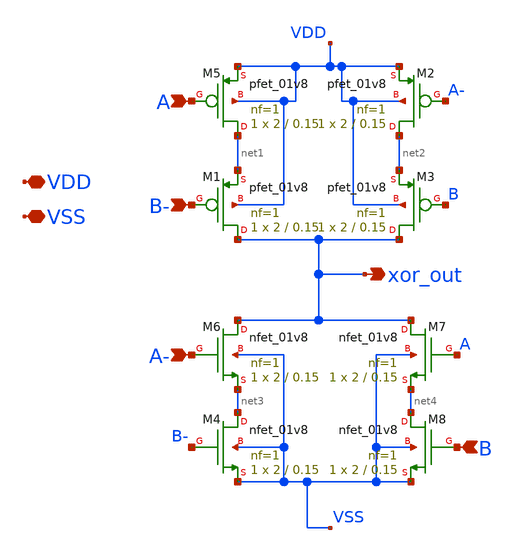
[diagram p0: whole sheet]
** sch_path: xschem/tuning/robs_xor_tune.sch
**.subckt robs_xor_tune xor_out A B- A- B VDD VSS
*.opin xor_out
*.ipin A
*.ipin B-
*.ipin A-
*.ipin B
*.iopin VDD
*.iopin VSS
XM5 net1 A VDD VDD sky130_fd_pr__pfet_01v8 L=0.15 W=2 nf=1 ad='int((nf+1)/2) * W/nf * 0.29' as='int((nf+2)/2) * W/nf * 0.29'
+ pd='2*int((nf+1)/2) * (W/nf + 0.29)' ps='2*int((nf+2)/2) * (W/nf + 0.29)' nrd='0.29 / W' nrs='0.29 / W'
+ sa=0 sb=0 sd=0 mult=1 m=1
XM6 xor_out A- net3 VSS sky130_fd_pr__nfet_01v8 L=0.15 W=2 nf=1 ad='int((nf+1)/2) * W/nf * 0.29' as='int((nf+2)/2) * W/nf * 0.29'
+ pd='2*int((nf+1)/2) * (W/nf + 0.29)' ps='2*int((nf+2)/2) * (W/nf + 0.29)' nrd='0.29 / W' nrs='0.29 / W'
+ sa=0 sb=0 sd=0 mult=1 m=1
XM1 xor_out B- net1 VDD sky130_fd_pr__pfet_01v8 L=0.15 W=2 nf=1 ad='int((nf+1)/2) * W/nf * 0.29' as='int((nf+2)/2) * W/nf * 0.29'
+ pd='2*int((nf+1)/2) * (W/nf + 0.29)' ps='2*int((nf+2)/2) * (W/nf + 0.29)' nrd='0.29 / W' nrs='0.29 / W'
+ sa=0 sb=0 sd=0 mult=1 m=1
XM2 net2 A- VDD VDD sky130_fd_pr__pfet_01v8 L=0.15 W=2 nf=1 ad='int((nf+1)/2) * W/nf * 0.29' as='int((nf+2)/2) * W/nf * 0.29'
+ pd='2*int((nf+1)/2) * (W/nf + 0.29)' ps='2*int((nf+2)/2) * (W/nf + 0.29)' nrd='0.29 / W' nrs='0.29 / W'
+ sa=0 sb=0 sd=0 mult=1 m=1
XM3 xor_out B net2 VDD sky130_fd_pr__pfet_01v8 L=0.15 W=2 nf=1 ad='int((nf+1)/2) * W/nf * 0.29' as='int((nf+2)/2) * W/nf * 0.29'
+ pd='2*int((nf+1)/2) * (W/nf + 0.29)' ps='2*int((nf+2)/2) * (W/nf + 0.29)' nrd='0.29 / W' nrs='0.29 / W'
+ sa=0 sb=0 sd=0 mult=1 m=1
XM4 net3 B- VSS VSS sky130_fd_pr__nfet_01v8 L=0.15 W=2 nf=1 ad='int((nf+1)/2) * W/nf * 0.29' as='int((nf+2)/2) * W/nf * 0.29'
+ pd='2*int((nf+1)/2) * (W/nf + 0.29)' ps='2*int((nf+2)/2) * (W/nf + 0.29)' nrd='0.29 / W' nrs='0.29 / W'
+ sa=0 sb=0 sd=0 mult=1 m=1
XM7 xor_out A net4 VSS sky130_fd_pr__nfet_01v8 L=0.15 W=2 nf=1 ad='int((nf+1)/2) * W/nf * 0.29' as='int((nf+2)/2) * W/nf * 0.29'
+ pd='2*int((nf+1)/2) * (W/nf + 0.29)' ps='2*int((nf+2)/2) * (W/nf + 0.29)' nrd='0.29 / W' nrs='0.29 / W'
+ sa=0 sb=0 sd=0 mult=1 m=1
XM8 net4 B VSS VSS sky130_fd_pr__nfet_01v8 L=0.15 W=2 nf=1 ad='int((nf+1)/2) * W/nf * 0.29' as='int((nf+2)/2) * W/nf * 0.29'
+ pd='2*int((nf+1)/2) * (W/nf + 0.29)' ps='2*int((nf+2)/2) * (W/nf + 0.29)' nrd='0.29 / W' nrs='0.29 / W'
+ sa=0 sb=0 sd=0 mult=1 m=1
**.ends
.end
